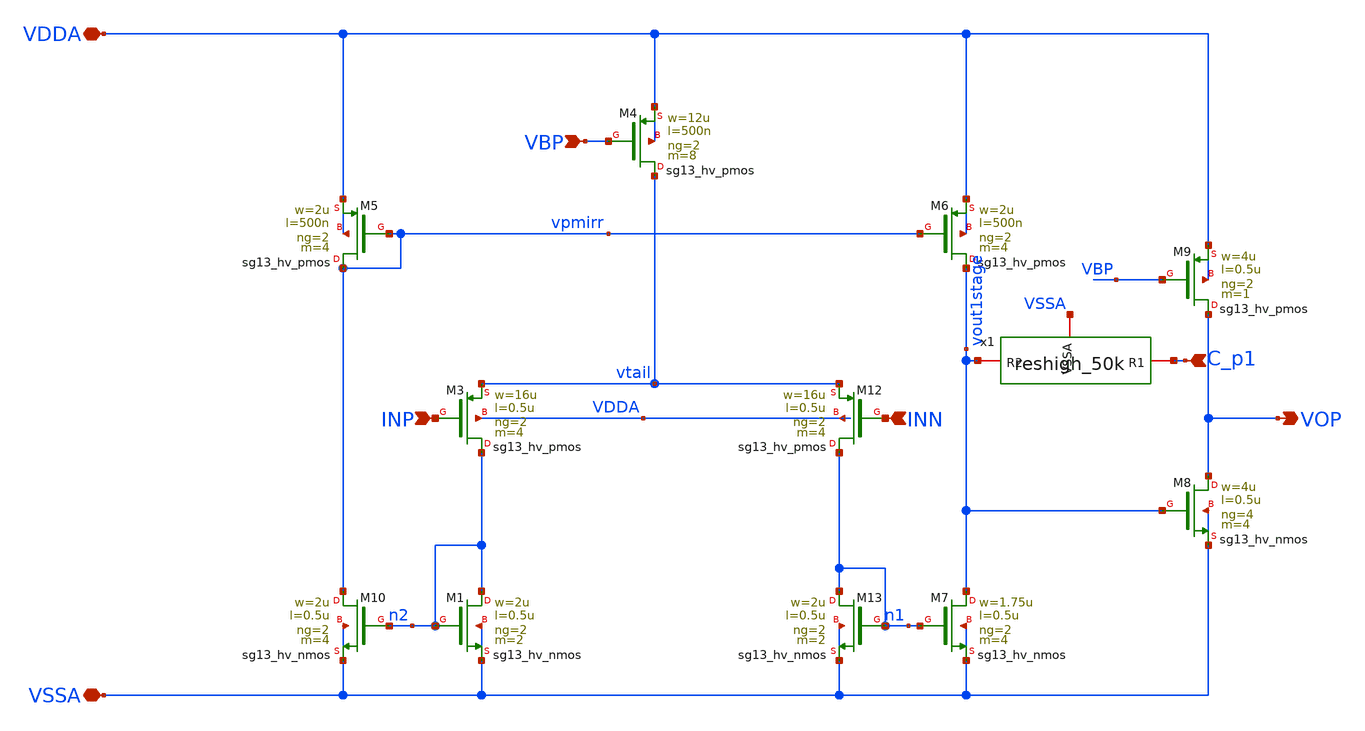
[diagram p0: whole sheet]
** sch_path: OTA_bc.sch
**.subckt OTA_bc VBP INP INN VSSA VDDA VOP C_p1
*.ipin VBP
*.ipin INP
*.ipin INN
*.iopin VSSA
*.iopin VDDA
*.opin VOP
*.ipin C_p1
XM13 n1 n1 VSSA VSSA sg13_hv_nmos w=2u l=0.5u ng=2 m=2 mm_ok=1
XM1 n2 n2 VSSA VSSA sg13_hv_nmos w=2u l=0.5u ng=2 m=2 mm_ok=1
XM12 n1 INN vtail VDDA sg13_hv_pmos w=16u l=0.5u ng=2 m=4 mm_ok=1
XM3 n2 INP vtail VDDA sg13_hv_pmos w=16u l=0.5u ng=2 m=4 mm_ok=1
XM4 vtail VBP VDDA VDDA sg13_hv_pmos w=12u l=500n ng=2 m=8 mm_ok=1
XM5 vpmirr vpmirr VDDA VDDA sg13_hv_pmos w=2u l=500n ng=2 m=4 mm_ok=1
XM6 vout1stage vpmirr VDDA VDDA sg13_hv_pmos w=2u l=500n ng=2 m=4 mm_ok=1
XM7 vout1stage n1 VSSA VSSA sg13_hv_nmos w=1.75u l=0.5u ng=2 m=4 mm_ok=1
XM8 VOP vout1stage VSSA VSSA sg13_hv_nmos w=4u l=0.5u ng=4 m=4 mm_ok=1
XM9 VOP VBP VDDA VDDA sg13_hv_pmos w=4u l=0.5u ng=2 m=1 mm_ok=1
XM10 vpmirr n2 VSSA VSSA sg13_hv_nmos w=2u l=0.5u ng=2 m=4 mm_ok=1
x1 C_p1 vout1stage VSSA reshigh_50k
**.ends

* expanding   symbol:  reshigh_50k.sym # of pins=3
** sym_path: reshigh_50k.sym
** sch_path: reshigh_50k.sch
.subckt reshigh_50k R1 R2 VSSA
*.iopin R2
*.iopin R1
*.iopin VSSA
XR1 R2 R1 VSSA rhigh w=0.5e-6 l=16.75e-6 m=1 b=0 mm_ok=1
.ends

.end
